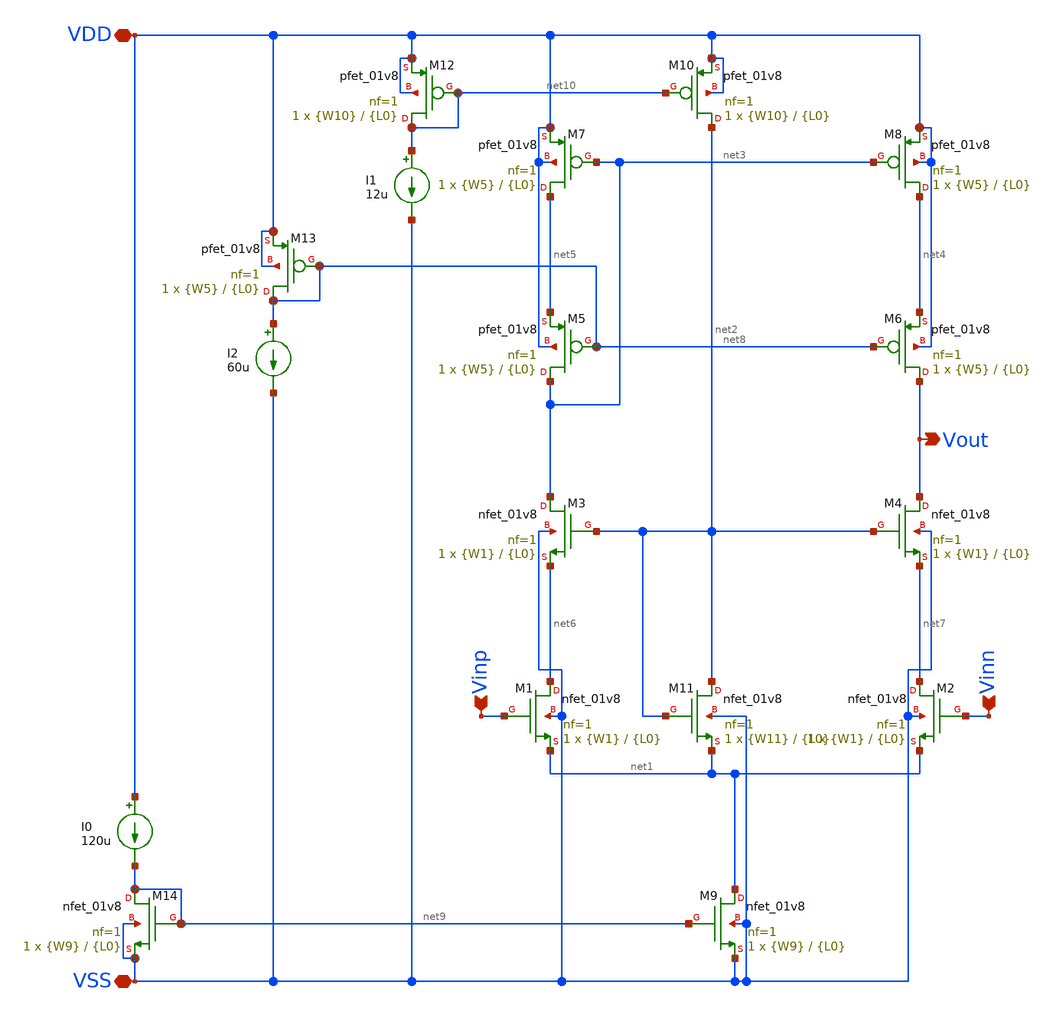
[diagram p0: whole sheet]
** sch_path: opamp_design/cascode_one_stage_opamp/cascode_one_stage_opamp.sch
**.subckt cascode_one_stage_opamp Vinp Vinn Vout VDD VSS
*.ipin Vinp
*.ipin Vinn
*.opin Vout
*.iopin VDD
*.iopin VSS
XM1 net6 Vinp net1 VSS sky130_fd_pr__nfet_01v8 L={L0} W={W1} nf=1 ad='int((nf+1)/2) * W/nf * 0.29' as='int((nf+2)/2) * W/nf * 0.29'
+ pd='2*int((nf+1)/2) * (W/nf + 0.29)' ps='2*int((nf+2)/2) * (W/nf + 0.29)' nrd='0.29 / W' nrs='0.29 / W'
+ sa=0 sb=0 sd=0 mult=1 m=1
XM2 net7 Vinn net1 VSS sky130_fd_pr__nfet_01v8 L={L0} W={W1} nf=1 ad='int((nf+1)/2) * W/nf * 0.29' as='int((nf+2)/2) * W/nf * 0.29'
+ pd='2*int((nf+1)/2) * (W/nf + 0.29)' ps='2*int((nf+2)/2) * (W/nf + 0.29)' nrd='0.29 / W' nrs='0.29 / W'
+ sa=0 sb=0 sd=0 mult=1 m=1
XM9 net1 net9 VSS VSS sky130_fd_pr__nfet_01v8 L={L0} W={W9} nf=1 ad='int((nf+1)/2) * W/nf * 0.29' as='int((nf+2)/2) * W/nf * 0.29'
+ pd='2*int((nf+1)/2) * (W/nf + 0.29)' ps='2*int((nf+2)/2) * (W/nf + 0.29)' nrd='0.29 / W' nrs='0.29 / W'
+ sa=0 sb=0 sd=0 mult=1 m=1
XM11 net2 net2 net1 VSS sky130_fd_pr__nfet_01v8 L={L0} W={W11} nf=1 ad='int((nf+1)/2) * W/nf * 0.29'
+ as='int((nf+2)/2) * W/nf * 0.29' pd='2*int((nf+1)/2) * (W/nf + 0.29)' ps='2*int((nf+2)/2) * (W/nf + 0.29)'
+ nrd='0.29 / W' nrs='0.29 / W' sa=0 sb=0 sd=0 mult=1 m=1
XM3 net3 net2 net6 VSS sky130_fd_pr__nfet_01v8 L={L0} W={W1} nf=1 ad='int((nf+1)/2) * W/nf * 0.29' as='int((nf+2)/2) * W/nf * 0.29'
+ pd='2*int((nf+1)/2) * (W/nf + 0.29)' ps='2*int((nf+2)/2) * (W/nf + 0.29)' nrd='0.29 / W' nrs='0.29 / W'
+ sa=0 sb=0 sd=0 mult=1 m=1
XM4 Vout net2 net7 VSS sky130_fd_pr__nfet_01v8 L={L0} W={W1} nf=1 ad='int((nf+1)/2) * W/nf * 0.29' as='int((nf+2)/2) * W/nf * 0.29'
+ pd='2*int((nf+1)/2) * (W/nf + 0.29)' ps='2*int((nf+2)/2) * (W/nf + 0.29)' nrd='0.29 / W' nrs='0.29 / W'
+ sa=0 sb=0 sd=0 mult=1 m=1
XM6 Vout net8 net4 VDD sky130_fd_pr__pfet_01v8 L={L0} W={W5} nf=1 ad='int((nf+1)/2) * W/nf * 0.29' as='int((nf+2)/2) * W/nf * 0.29'
+ pd='2*int((nf+1)/2) * (W/nf + 0.29)' ps='2*int((nf+2)/2) * (W/nf + 0.29)' nrd='0.29 / W' nrs='0.29 / W'
+ sa=0 sb=0 sd=0 mult=1 m=1
XM5 net3 net8 net5 VDD sky130_fd_pr__pfet_01v8 L={L0} W={W5} nf=1 ad='int((nf+1)/2) * W/nf * 0.29' as='int((nf+2)/2) * W/nf * 0.29'
+ pd='2*int((nf+1)/2) * (W/nf + 0.29)' ps='2*int((nf+2)/2) * (W/nf + 0.29)' nrd='0.29 / W' nrs='0.29 / W'
+ sa=0 sb=0 sd=0 mult=1 m=1
XM7 net5 net3 VDD VDD sky130_fd_pr__pfet_01v8 L={L0} W={W5} nf=1 ad='int((nf+1)/2) * W/nf * 0.29' as='int((nf+2)/2) * W/nf * 0.29'
+ pd='2*int((nf+1)/2) * (W/nf + 0.29)' ps='2*int((nf+2)/2) * (W/nf + 0.29)' nrd='0.29 / W' nrs='0.29 / W'
+ sa=0 sb=0 sd=0 mult=1 m=1
XM8 net4 net3 VDD VDD sky130_fd_pr__pfet_01v8 L={L0} W={W5} nf=1 ad='int((nf+1)/2) * W/nf * 0.29' as='int((nf+2)/2) * W/nf * 0.29'
+ pd='2*int((nf+1)/2) * (W/nf + 0.29)' ps='2*int((nf+2)/2) * (W/nf + 0.29)' nrd='0.29 / W' nrs='0.29 / W'
+ sa=0 sb=0 sd=0 mult=1 m=1
XM10 net2 net10 VDD VDD sky130_fd_pr__pfet_01v8 L={L0} W={W10} nf=1 ad='int((nf+1)/2) * W/nf * 0.29'
+ as='int((nf+2)/2) * W/nf * 0.29' pd='2*int((nf+1)/2) * (W/nf + 0.29)' ps='2*int((nf+2)/2) * (W/nf + 0.29)'
+ nrd='0.29 / W' nrs='0.29 / W' sa=0 sb=0 sd=0 mult=1 m=1
XM14 net9 net9 VSS VSS sky130_fd_pr__nfet_01v8 L={L0} W={W9} nf=1 ad='int((nf+1)/2) * W/nf * 0.29' as='int((nf+2)/2) * W/nf * 0.29'
+ pd='2*int((nf+1)/2) * (W/nf + 0.29)' ps='2*int((nf+2)/2) * (W/nf + 0.29)' nrd='0.29 / W' nrs='0.29 / W'
+ sa=0 sb=0 sd=0 mult=1 m=1
I0 VDD net9 120u
I1 net10 VSS 12u
XM12 net10 net10 VDD VDD sky130_fd_pr__pfet_01v8 L={L0} W={W10} nf=1 ad='int((nf+1)/2) * W/nf * 0.29'
+ as='int((nf+2)/2) * W/nf * 0.29' pd='2*int((nf+1)/2) * (W/nf + 0.29)' ps='2*int((nf+2)/2) * (W/nf + 0.29)'
+ nrd='0.29 / W' nrs='0.29 / W' sa=0 sb=0 sd=0 mult=1 m=1
I2 net8 VSS 60u
XM13 net8 net8 VDD VDD sky130_fd_pr__pfet_01v8 L={L0} W={W5} nf=1 ad='int((nf+1)/2) * W/nf * 0.29' as='int((nf+2)/2) * W/nf * 0.29'
+ pd='2*int((nf+1)/2) * (W/nf + 0.29)' ps='2*int((nf+2)/2) * (W/nf + 0.29)' nrd='0.29 / W' nrs='0.29 / W'
+ sa=0 sb=0 sd=0 mult=1 m=1
**.ends
.end
